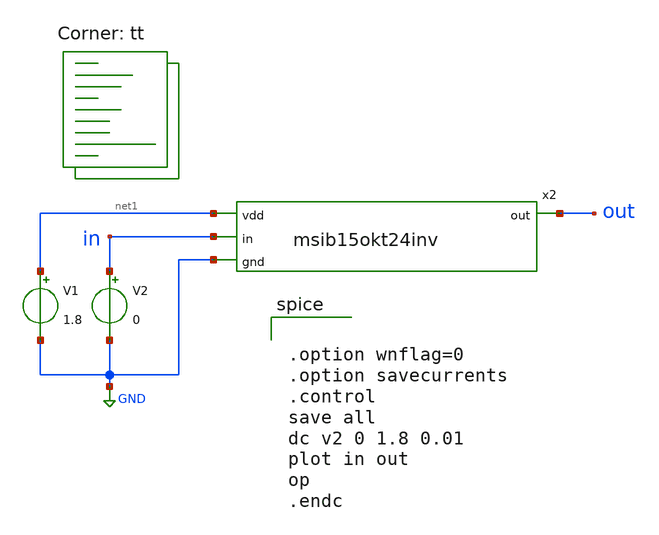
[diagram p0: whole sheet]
** sch_path: Inverter/SCH/msib15okt24invtb.sch
**.subckt msib15okt24invtb
V1 net1 GND 1.8
V2 in GND 0
x2 net1 in out GND msib15okt24inv
**** begin user architecture code
.lib $::SKYWATER_MODELS/sky130.lib.spice tt


.option wnflag=0
.option savecurrents
.control
save all
dc v2 0 1.8 0.01
plot in out
op
.endc


**** end user architecture code
**.ends
.GLOBAL GND
.end
